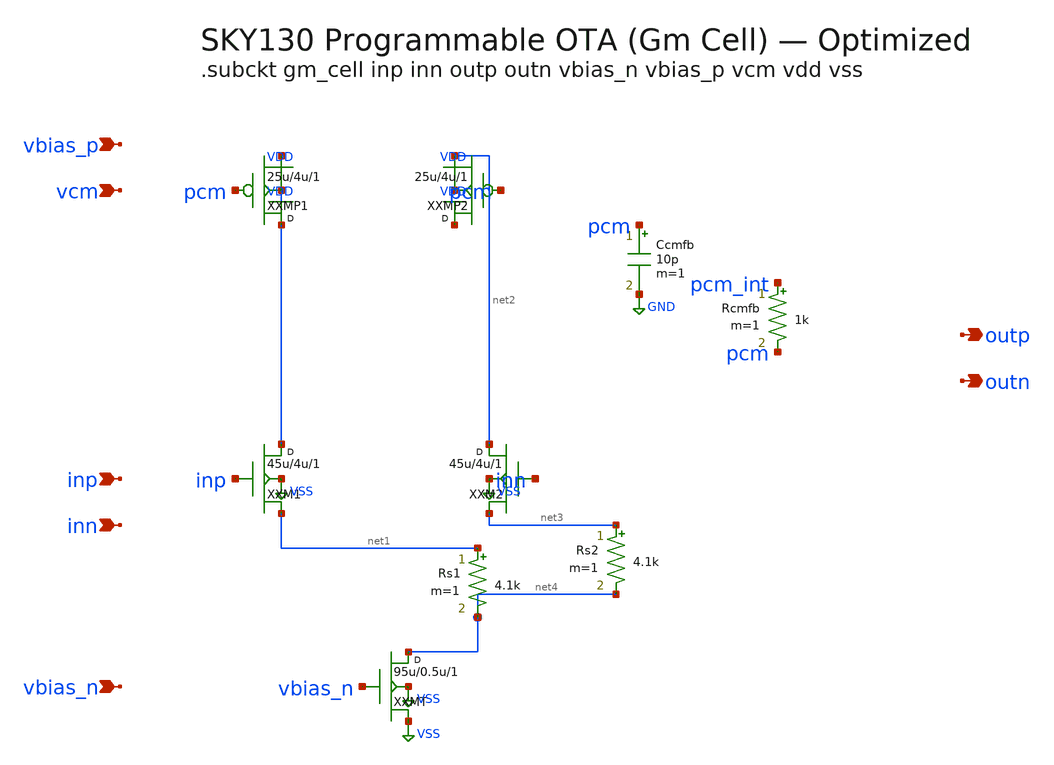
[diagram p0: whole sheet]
** sch_path: data/sch/ode_gm-cell.sch
**.subckt ode_gm-cell inp inn vbias_n vbias_p vcm outp outn
*.ipin inp
*.ipin inn
*.ipin vbias_n
*.ipin vbias_p
*.ipin vcm
*.opin outp
*.opin outn
XXM1 VDD inp net1 VSS sky130_fd_pr__nfet_01v8 w=45u l=4u m=1
XXM2 net2 inn net3 VSS sky130_fd_pr__nfet_01v8 w=45u l=4u m=1
Rs1 net1 net4 4.1k m=1
Rs2 net3 net4 4.1k m=1
XXMT net4 vbias_n VSS VSS sky130_fd_pr__nfet_01v8 w=95u l=0.5u m=1
XXMP1 VDD pcm VDD VDD sky130_fd_pr__pfet_01v8 w=25u l=4u m=1
XXMP2 VDD pcm net2 VDD sky130_fd_pr__pfet_01v8 w=25u l=4u m=1
Rcmfb pcm_int pcm 1k m=1
Ccmfb pcm GND 10p m=1
**.ends
.GLOBAL VSS
.GLOBAL VDD
.GLOBAL GND
.end
